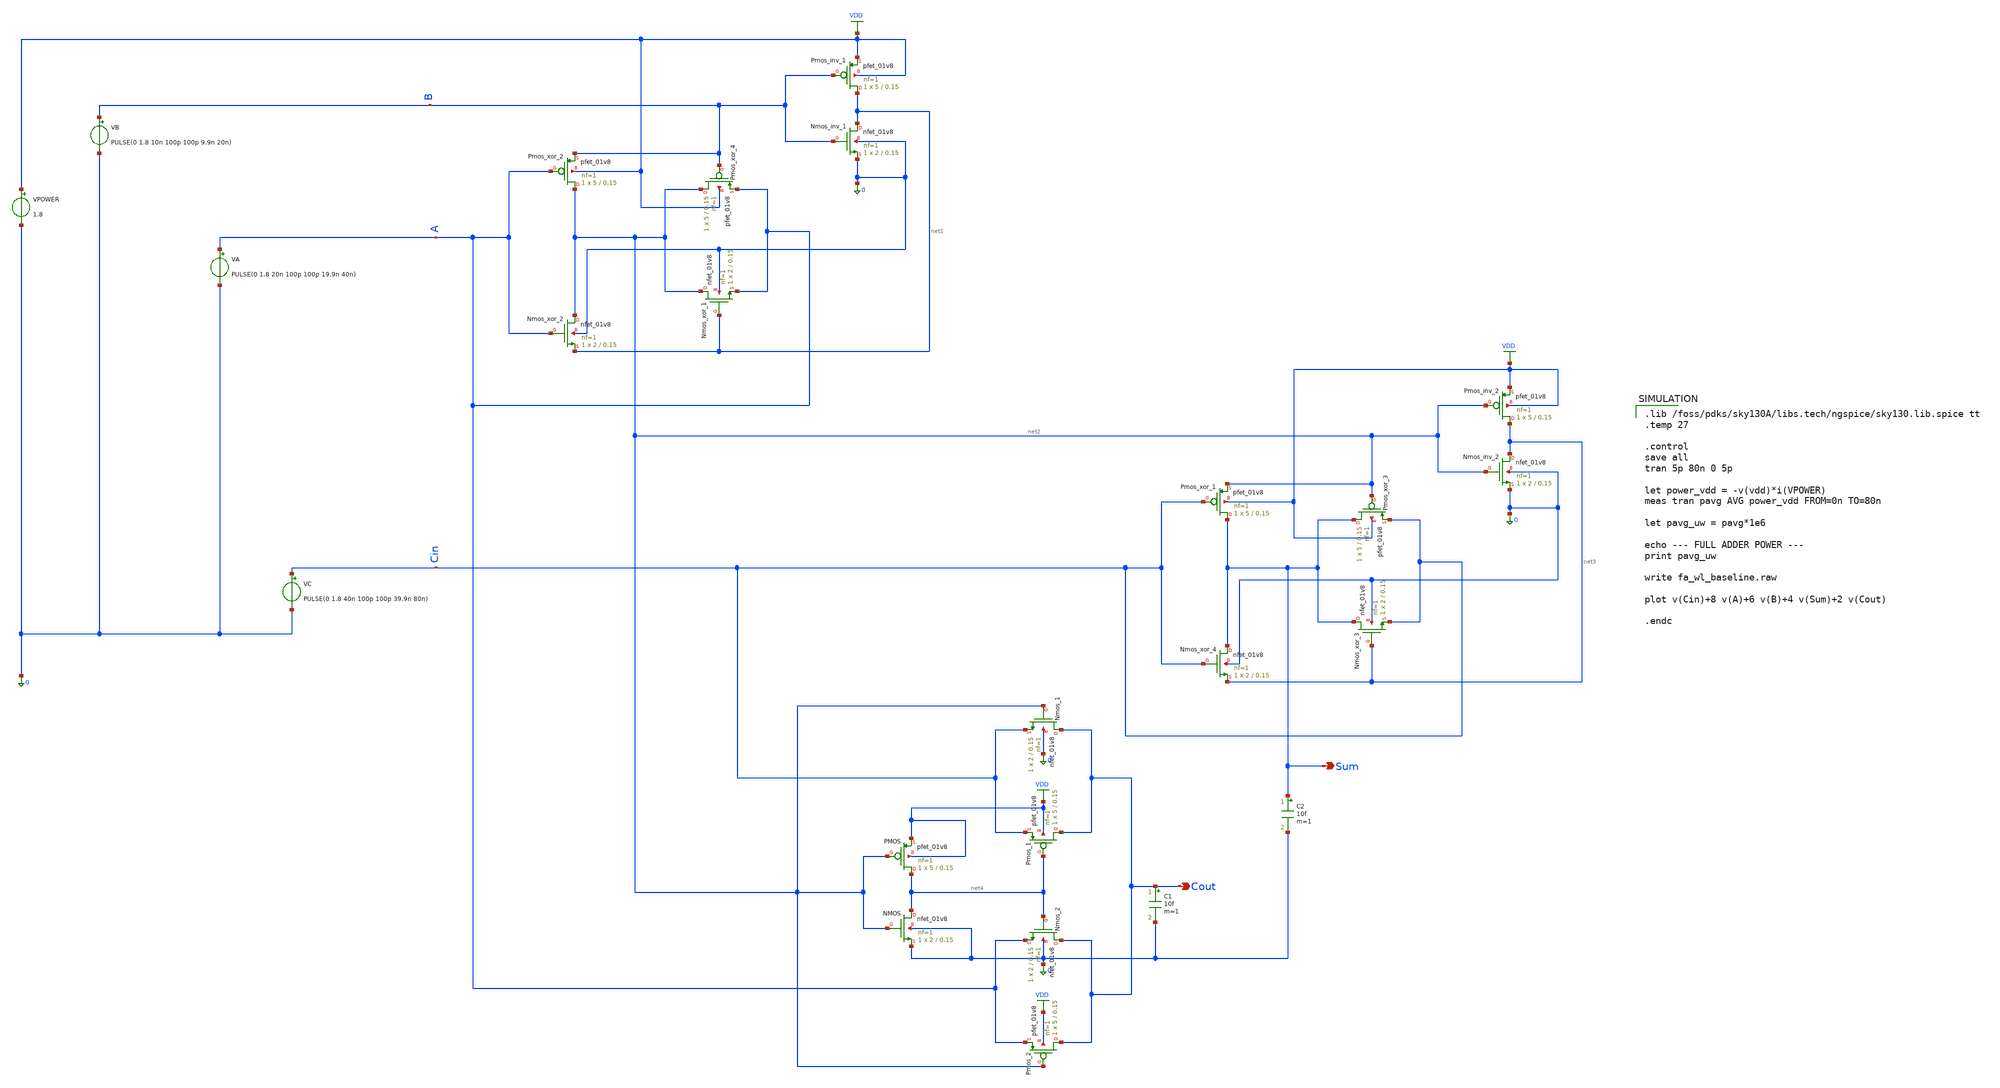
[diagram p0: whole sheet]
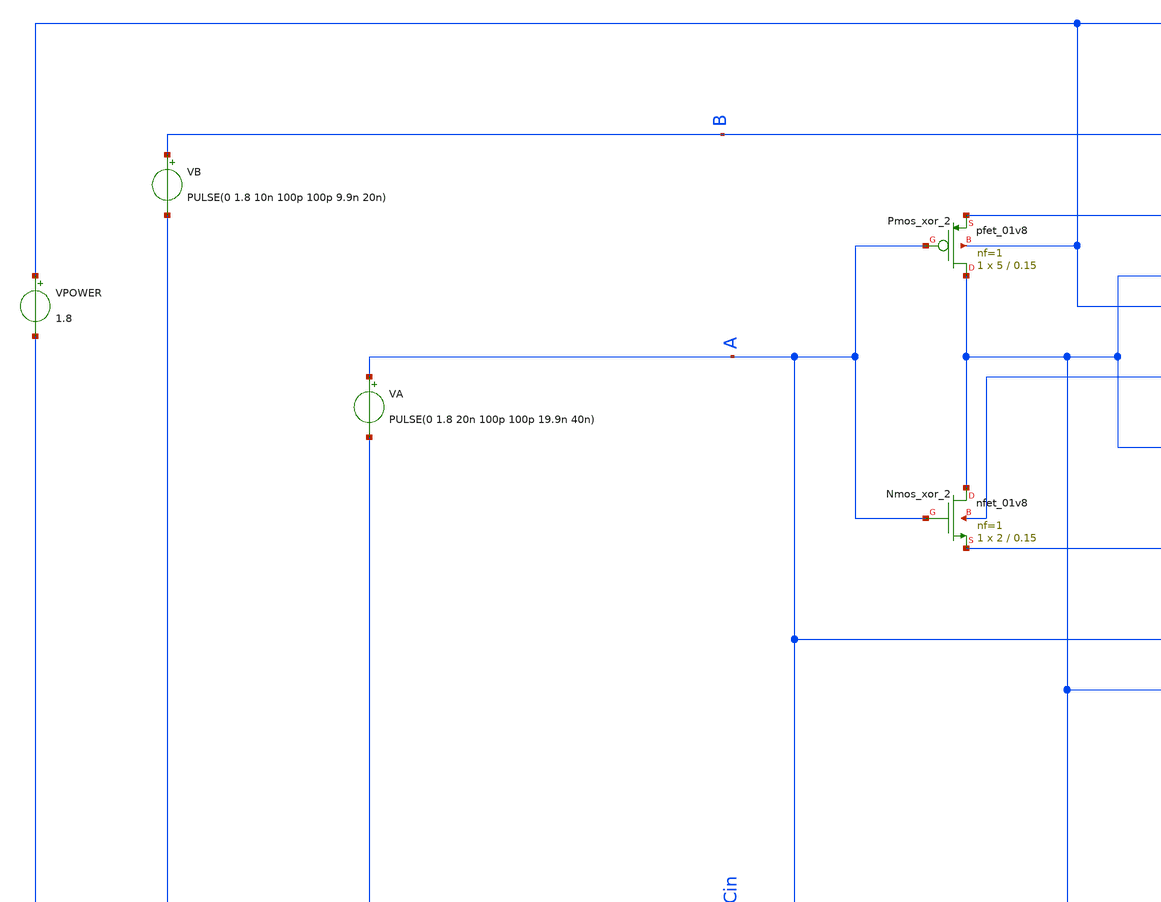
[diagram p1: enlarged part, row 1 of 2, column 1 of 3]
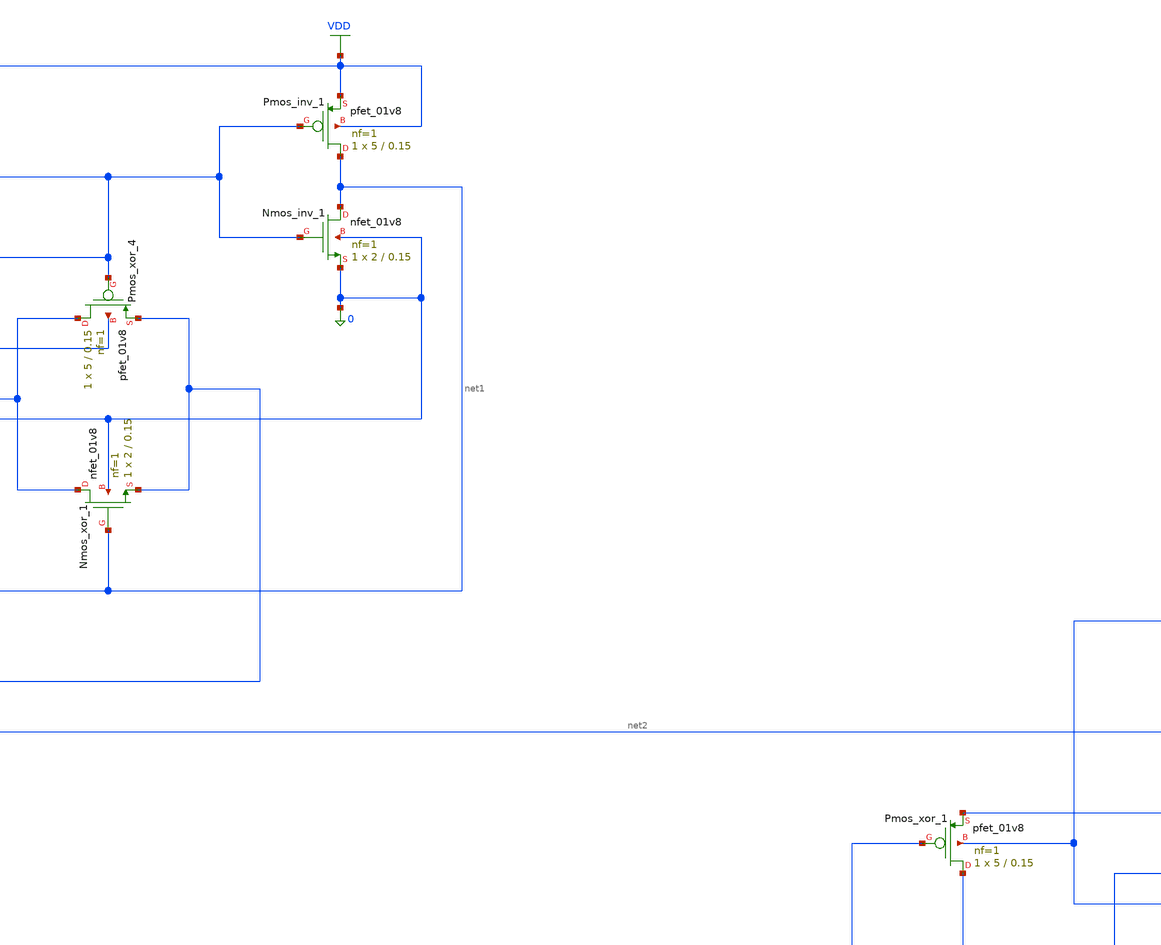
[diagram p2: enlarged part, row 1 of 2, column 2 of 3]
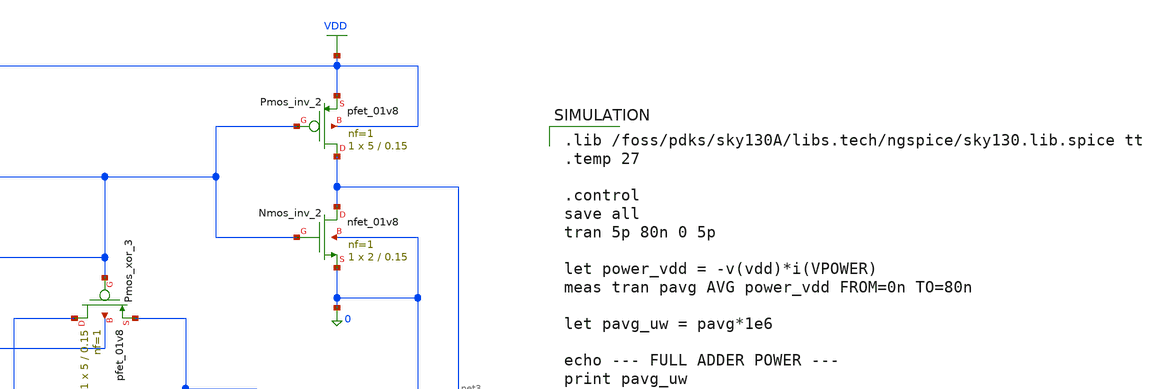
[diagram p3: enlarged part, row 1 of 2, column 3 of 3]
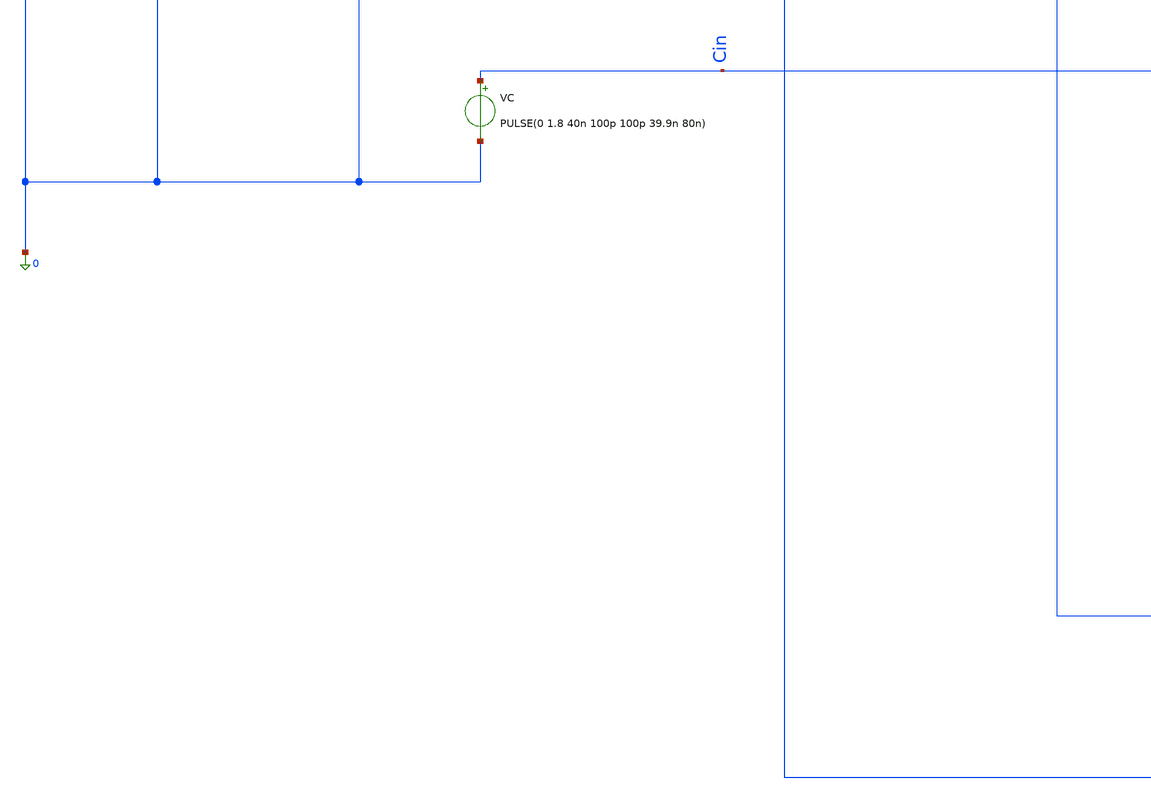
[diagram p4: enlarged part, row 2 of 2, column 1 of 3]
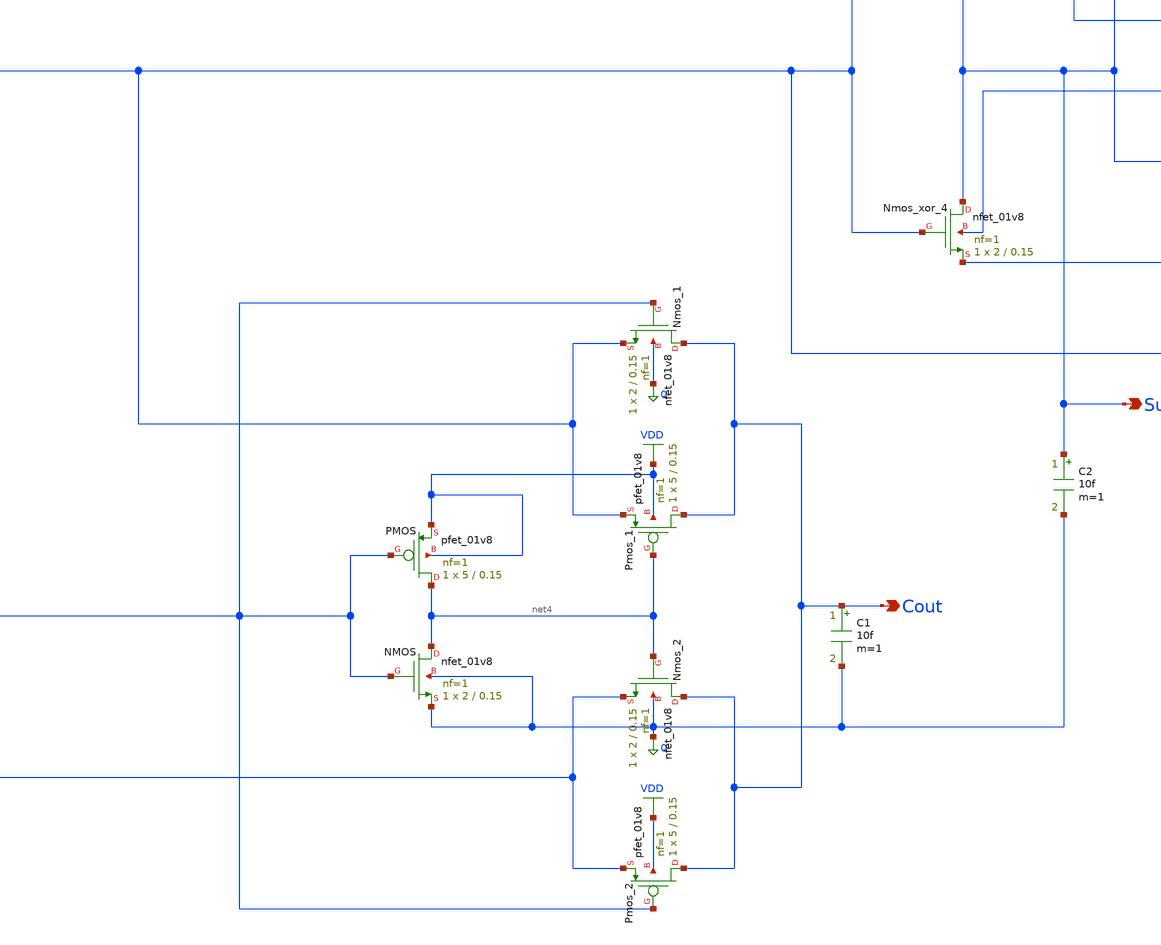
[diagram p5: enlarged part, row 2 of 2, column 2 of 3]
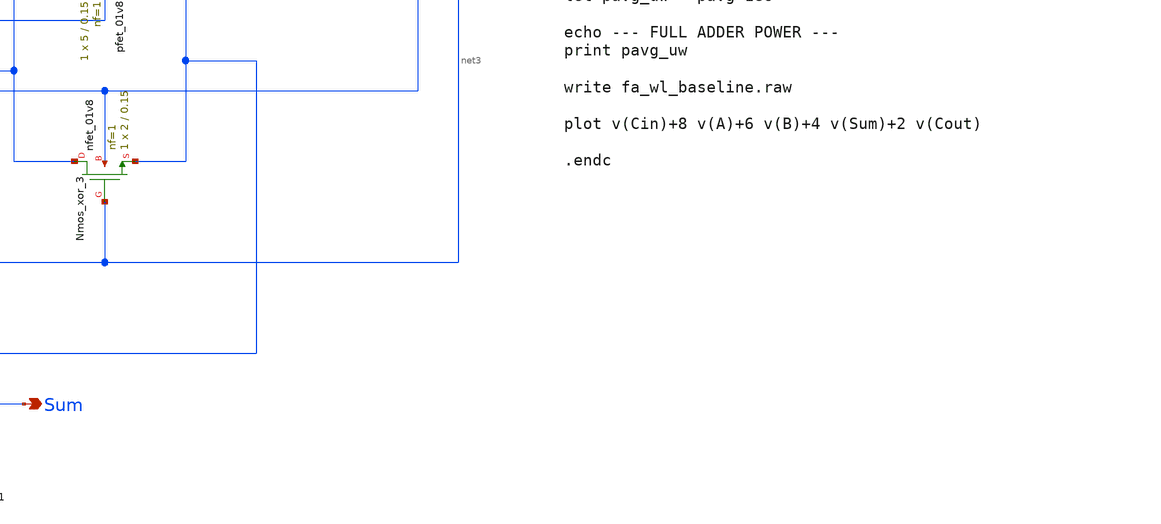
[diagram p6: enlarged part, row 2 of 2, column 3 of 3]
** sch_path: cells/full_adder_tg/xschem/FA_TG_WL_sweep.sch
**.subckt FA_TG_WL_sweep Sum Cout
*.opin Sum
*.opin Cout
XPmos_inv_1 net1 B VDD VDD sky130_fd_pr__pfet_01v8 L=0.15 W=5 nf=1 ad='int((1 + 1)/2) * 5 / 1 * 0.29'
+ as='int((1 + 2)/2) * 5 / 1 * 0.29' pd='2*int((1 + 1)/2) * (5 / 1 + 0.29)' ps='2*int((1 + 2)/2) * (5 / 1 + 0.29)'
+ nrd='0.29 / 5 ' nrs='0.29 / 5 ' sa=0 sb=0 sd=0 mult=1 m=1
XNmos_inv_1 net1 B 0 0 sky130_fd_pr__nfet_01v8 L=0.15 W=2 nf=1 ad='int((1 + 1)/2) * 2 / 1 * 0.29' as='int((1 + 2)/2) * 2 / 1 * 0.29'
+ pd='2*int((1 + 1)/2) * (2 / 1 + 0.29)' ps='2*int((1 + 2)/2) * (2 / 1 + 0.29)' nrd='0.29 / 2 ' nrs='0.29 / 2 '
+ sa=0 sb=0 sd=0 mult=1 m=1
XPmos_xor_4 net2 B A VDD sky130_fd_pr__pfet_01v8 L=0.15 W=5 nf=1 ad='int((1 + 1)/2) * 5 / 1 * 0.29' as='int((1 + 2)/2) * 5 / 1 * 0.29'
+ pd='2*int((1 + 1)/2) * (5 / 1 + 0.29)' ps='2*int((1 + 2)/2) * (5 / 1 + 0.29)' nrd='0.29 / 5 ' nrs='0.29 / 5 '
+ sa=0 sb=0 sd=0 mult=1 m=1
XNmos_xor_1 net2 net1 A 0 sky130_fd_pr__nfet_01v8 L=0.15 W=2 nf=1 ad='int((1 + 1)/2) * 2 / 1 * 0.29'
+ as='int((1 + 2)/2) * 2 / 1 * 0.29' pd='2*int((1 + 1)/2) * (2 / 1 + 0.29)' ps='2*int((1 + 2)/2) * (2 / 1 + 0.29)'
+ nrd='0.29 / 2 ' nrs='0.29 / 2 ' sa=0 sb=0 sd=0 mult=1 m=1
XPmos_xor_2 net2 A B VDD sky130_fd_pr__pfet_01v8 L=0.15 W=5 nf=1 ad='int((1 + 1)/2) * 5 / 1 * 0.29' as='int((1 + 2)/2) * 5 / 1 * 0.29'
+ pd='2*int((1 + 1)/2) * (5 / 1 + 0.29)' ps='2*int((1 + 2)/2) * (5 / 1 + 0.29)' nrd='0.29 / 5 ' nrs='0.29 / 5 '
+ sa=0 sb=0 sd=0 mult=1 m=1
XNmos_xor_2 net2 A net1 0 sky130_fd_pr__nfet_01v8 L=0.15 W=2 nf=1 ad='int((1 + 1)/2) * 2 / 1 * 0.29'
+ as='int((1 + 2)/2) * 2 / 1 * 0.29' pd='2*int((1 + 1)/2) * (2 / 1 + 0.29)' ps='2*int((1 + 2)/2) * (2 / 1 + 0.29)'
+ nrd='0.29 / 2 ' nrs='0.29 / 2 ' sa=0 sb=0 sd=0 mult=1 m=1
XPmos_inv_2 net3 net2 VDD VDD sky130_fd_pr__pfet_01v8 L=0.15 W=5 nf=1 ad='int((1 + 1)/2) * 5 / 1 * 0.29'
+ as='int((1 + 2)/2) * 5 / 1 * 0.29' pd='2*int((1 + 1)/2) * (5 / 1 + 0.29)' ps='2*int((1 + 2)/2) * (5 / 1 + 0.29)'
+ nrd='0.29 / 5 ' nrs='0.29 / 5 ' sa=0 sb=0 sd=0 mult=1 m=1
XNmos_inv_2 net3 net2 0 0 sky130_fd_pr__nfet_01v8 L=0.15 W=2 nf=1 ad='int((1 + 1)/2) * 2 / 1 * 0.29'
+ as='int((1 + 2)/2) * 2 / 1 * 0.29' pd='2*int((1 + 1)/2) * (2 / 1 + 0.29)' ps='2*int((1 + 2)/2) * (2 / 1 + 0.29)'
+ nrd='0.29 / 2 ' nrs='0.29 / 2 ' sa=0 sb=0 sd=0 mult=1 m=1
XPmos_xor_3 Sum net2 Cin VDD sky130_fd_pr__pfet_01v8 L=0.15 W=5 nf=1 ad='int((1 + 1)/2) * 5 / 1 * 0.29'
+ as='int((1 + 2)/2) * 5 / 1 * 0.29' pd='2*int((1 + 1)/2) * (5 / 1 + 0.29)' ps='2*int((1 + 2)/2) * (5 / 1 + 0.29)'
+ nrd='0.29 / 5 ' nrs='0.29 / 5 ' sa=0 sb=0 sd=0 mult=1 m=1
XNmos_xor_3 Sum net3 Cin 0 sky130_fd_pr__nfet_01v8 L=0.15 W=2 nf=1 ad='int((1 + 1)/2) * 2 / 1 * 0.29'
+ as='int((1 + 2)/2) * 2 / 1 * 0.29' pd='2*int((1 + 1)/2) * (2 / 1 + 0.29)' ps='2*int((1 + 2)/2) * (2 / 1 + 0.29)'
+ nrd='0.29 / 2 ' nrs='0.29 / 2 ' sa=0 sb=0 sd=0 mult=1 m=1
XPmos_xor_1 Sum Cin net2 VDD sky130_fd_pr__pfet_01v8 L=0.15 W=5 nf=1 ad='int((1 + 1)/2) * 5 / 1 * 0.29'
+ as='int((1 + 2)/2) * 5 / 1 * 0.29' pd='2*int((1 + 1)/2) * (5 / 1 + 0.29)' ps='2*int((1 + 2)/2) * (5 / 1 + 0.29)'
+ nrd='0.29 / 5 ' nrs='0.29 / 5 ' sa=0 sb=0 sd=0 mult=1 m=1
XNmos_xor_4 Sum Cin net3 0 sky130_fd_pr__nfet_01v8 L=0.15 W=2 nf=1 ad='int((1 + 1)/2) * 2 / 1 * 0.29'
+ as='int((1 + 2)/2) * 2 / 1 * 0.29' pd='2*int((1 + 1)/2) * (2 / 1 + 0.29)' ps='2*int((1 + 2)/2) * (2 / 1 + 0.29)'
+ nrd='0.29 / 2 ' nrs='0.29 / 2 ' sa=0 sb=0 sd=0 mult=1 m=1
C2 Sum 0 10f m=1
XNmos_1 Cout net2 Cin 0 sky130_fd_pr__nfet_01v8 L=0.15 W=2 nf=1 ad='int((1 + 1)/2) * 2 / 1 * 0.29' as='int((1 + 2)/2) * 2 / 1 * 0.29'
+ pd='2*int((1 + 1)/2) * (2 / 1 + 0.29)' ps='2*int((1 + 2)/2) * (2 / 1 + 0.29)' nrd='0.29 / 2 ' nrs='0.29 / 2 '
+ sa=0 sb=0 sd=0 mult=1 m=1
XPmos_1 Cout net4 Cin VDD sky130_fd_pr__pfet_01v8 L=0.15 W=5 nf=1 ad='int((1 + 1)/2) * 5 / 1 * 0.29'
+ as='int((1 + 2)/2) * 5 / 1 * 0.29' pd='2*int((1 + 1)/2) * (5 / 1 + 0.29)' ps='2*int((1 + 2)/2) * (5 / 1 + 0.29)'
+ nrd='0.29 / 5 ' nrs='0.29 / 5 ' sa=0 sb=0 sd=0 mult=1 m=1
XNmos_2 Cout net4 A 0 sky130_fd_pr__nfet_01v8 L=0.15 W=2 nf=1 ad='int((1 + 1)/2) * 2 / 1 * 0.29' as='int((1 + 2)/2) * 2 / 1 * 0.29'
+ pd='2*int((1 + 1)/2) * (2 / 1 + 0.29)' ps='2*int((1 + 2)/2) * (2 / 1 + 0.29)' nrd='0.29 / 2 ' nrs='0.29 / 2 '
+ sa=0 sb=0 sd=0 mult=1 m=1
XPmos_2 Cout net2 A VDD sky130_fd_pr__pfet_01v8 L=0.15 W=5 nf=1 ad='int((1 + 1)/2) * 5 / 1 * 0.29' as='int((1 + 2)/2) * 5 / 1 * 0.29'
+ pd='2*int((1 + 1)/2) * (5 / 1 + 0.29)' ps='2*int((1 + 2)/2) * (5 / 1 + 0.29)' nrd='0.29 / 5 ' nrs='0.29 / 5 '
+ sa=0 sb=0 sd=0 mult=1 m=1
XNMOS net4 net2 0 0 sky130_fd_pr__nfet_01v8 L=0.15 W=2 nf=1 ad='int((1 + 1)/2) * 2 / 1 * 0.29' as='int((1 + 2)/2) * 2 / 1 * 0.29'
+ pd='2*int((1 + 1)/2) * (2 / 1 + 0.29)' ps='2*int((1 + 2)/2) * (2 / 1 + 0.29)' nrd='0.29 / 2 ' nrs='0.29 / 2 '
+ sa=0 sb=0 sd=0 mult=1 m=1
XPMOS net4 net2 VDD VDD sky130_fd_pr__pfet_01v8 L=0.15 W=5 nf=1 ad='int((1 + 1)/2) * 5 / 1 * 0.29' as='int((1 + 2)/2) * 5 / 1 * 0.29'
+ pd='2*int((1 + 1)/2) * (5 / 1 + 0.29)' ps='2*int((1 + 2)/2) * (5 / 1 + 0.29)' nrd='0.29 / 5 ' nrs='0.29 / 5 '
+ sa=0 sb=0 sd=0 mult=1 m=1
C1 Cout 0 10f m=1
VPOWER VDD 0 1.8
VB B 0 PULSE(0 1.8 10n 100p 100p 9.9n 20n)
VA A 0 PULSE(0 1.8 20n 100p 100p 19.9n 40n)
VC Cin 0 PULSE(0 1.8 40n 100p 100p 39.9n 80n)
**** begin user architecture code

.lib /foss/pdks/sky130A/libs.tech/ngspice/sky130.lib.spice tt
.temp 27

.control
save all
tran 5p 80n 0 5p

let power_vdd = -v(vdd)*i(VPOWER)
meas tran pavg AVG power_vdd FROM=0n TO=80n

let pavg_uw = pavg*1e6

echo --- FULL ADDER POWER ---
print pavg_uw

write fa_wl_baseline.raw

plot v(Cin)+8 v(A)+6 v(B)+4 v(Sum)+2 v(Cout)

.endc

**** end user architecture code
**.ends
.GLOBAL VDD
.end
